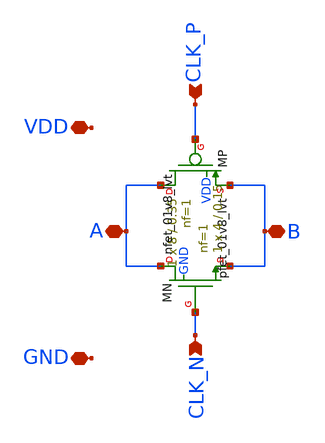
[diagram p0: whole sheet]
** sch_path: blocks/05_Switch_Network/xschem/TG_SC_LVT.sch
**.subckt TG_SC_LVT A B CLK_P CLK_N VDD GND
*.iopin A
*.iopin B
*.ipin CLK_P
*.ipin CLK_N
*.iopin VDD
*.iopin GND
XMP A CLK_P B VDD sky130_fd_pr__pfet_01v8_lvt L=0.35 W=8 nf=1 ad='int((1 + 1)/2) * 8 / 1 * 0.29' as='int((1 + 2)/2) * 8 / 1 * 0.29'
+ pd='2*int((1 + 1)/2) * (8 / 1 + 0.29)' ps='2*int((1 + 2)/2) * (8 / 1 + 0.29)' nrd='0.29 / 8 ' nrs='0.29 / 8 '
+ sa=0 sb=0 sd=0 mult=1
XMN A CLK_N B GND sky130_fd_pr__nfet_01v8_lvt L=0.15 W=4 nf=1 ad='int((1 + 1)/2) * 4 / 1 * 0.29' as='int((1 + 2)/2) * 4 / 1 * 0.29'
+ pd='2*int((1 + 1)/2) * (4 / 1 + 0.29)' ps='2*int((1 + 2)/2) * (4 / 1 + 0.29)' nrd='0.29 / 4 ' nrs='0.29 / 4 '
+ sa=0 sb=0 sd=0 mult=1
**.ends
.end
